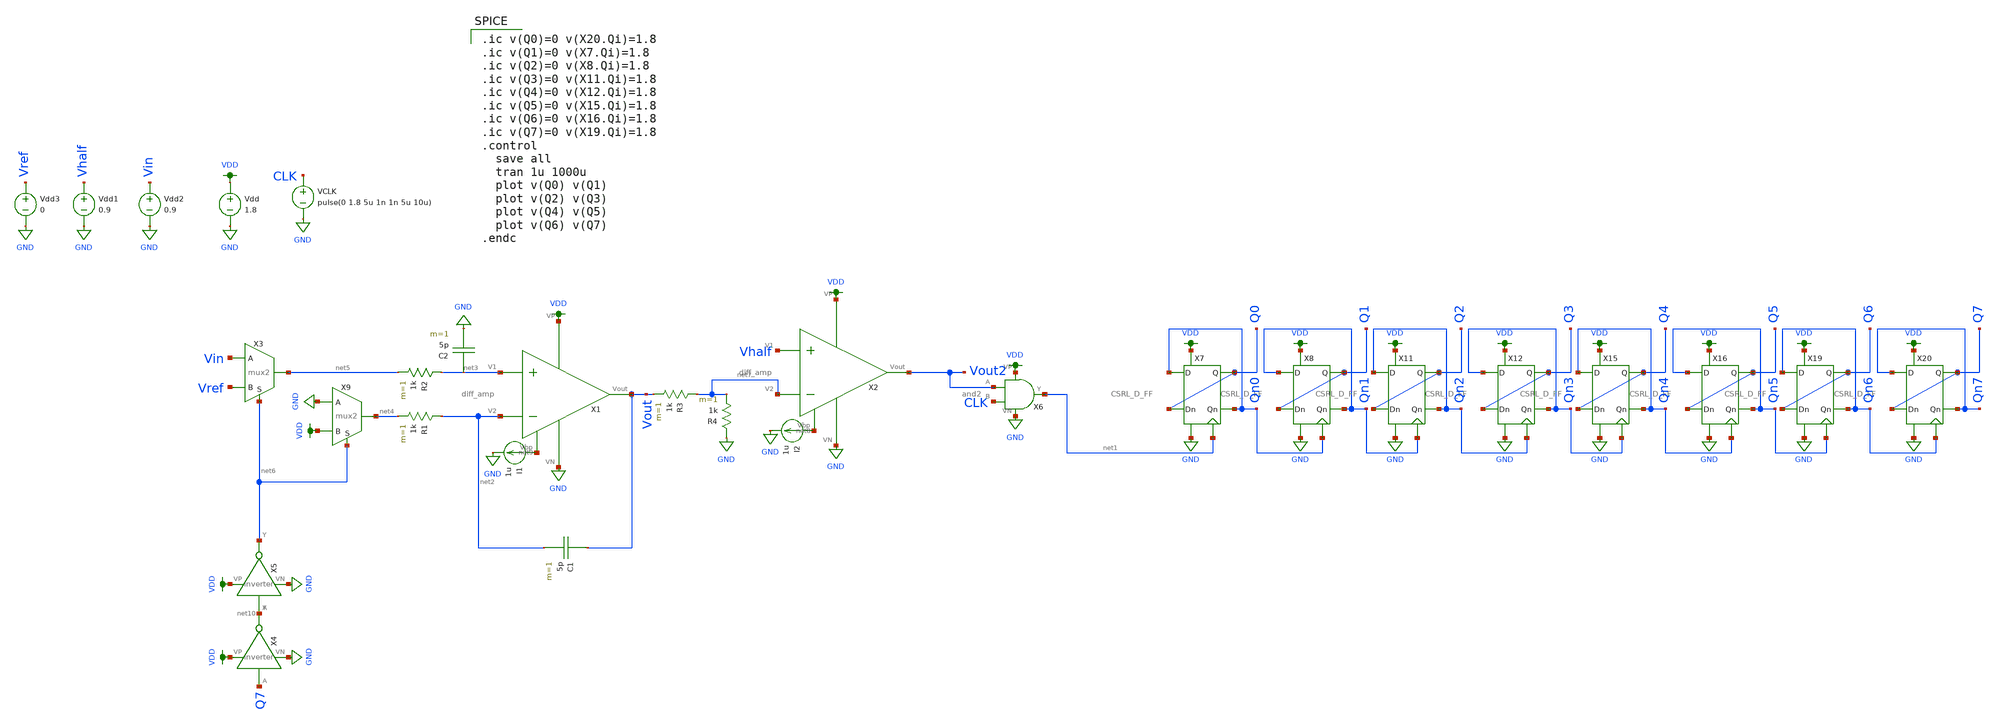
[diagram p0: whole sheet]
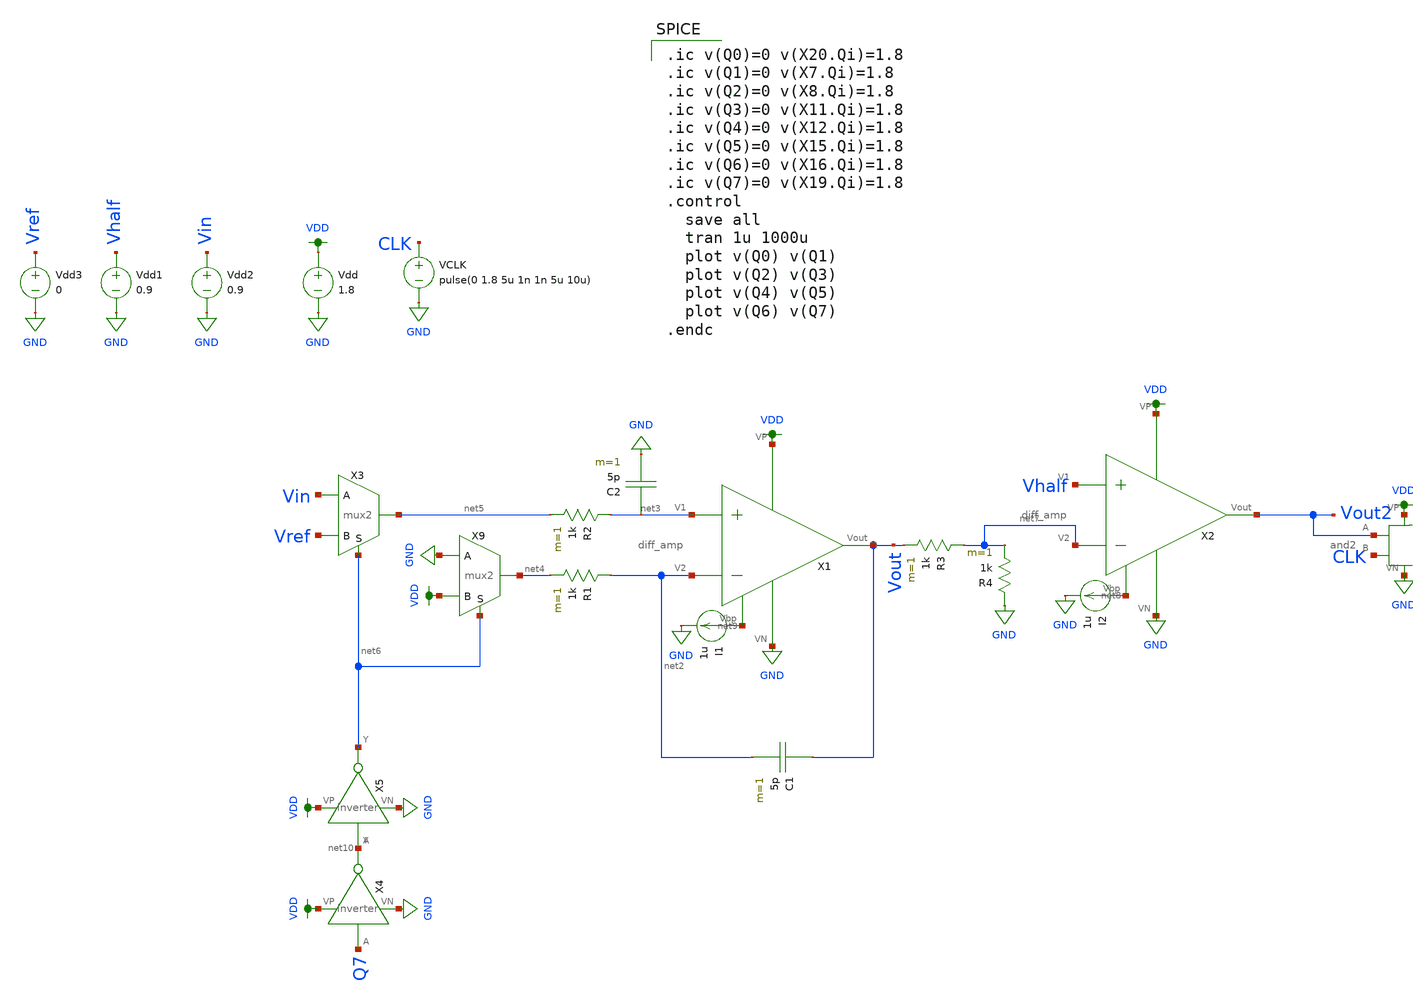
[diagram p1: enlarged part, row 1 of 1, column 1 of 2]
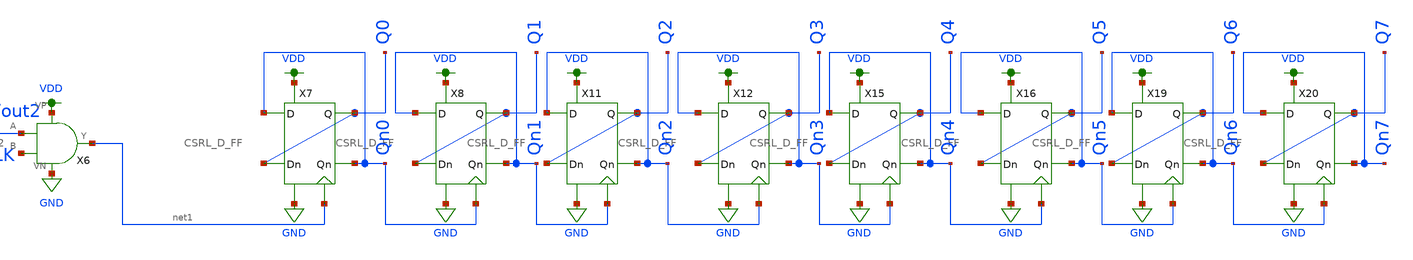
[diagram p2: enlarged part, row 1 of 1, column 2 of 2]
** sch_path: schematic/archive/double-slope-thomas.sch
**.subckt double-slope-thomas
X2 VDD net8 Vout2 Vhalf net7 GND diff_amp
Vdd VDD GND 1.8
VCLK CLK GND pulse(0 1.8 5u 1n 1n 5u 10u)
Vdd1 Vhalf GND 0.9
Vdd2 Vin GND 0.9
X7 Q0 Qn0 Qn0 Q0 GND VDD net1 CSRL_D_FF
X8 Q1 Qn1 Qn1 Q1 GND VDD Qn0 CSRL_D_FF
X11 Q2 Qn2 Qn2 Q2 GND VDD Qn1 CSRL_D_FF
X12 Q3 Qn3 Qn3 Q3 GND VDD Qn2 CSRL_D_FF
X15 Q4 Qn4 Qn4 Q4 GND VDD Qn3 CSRL_D_FF
X16 Q5 Qn5 Qn5 Q5 GND VDD Qn4 CSRL_D_FF
X19 Q6 Qn6 Qn6 Q6 GND VDD Qn5 CSRL_D_FF
X20 Q7 Qn7 Qn7 Q7 GND VDD Qn6 CSRL_D_FF
I2 net8 GND 1u
C1 Vout net2 5p m=1
X1 VDD net9 Vout net3 net2 GND diff_amp
R1 net2 net4 1k m=1
C2 net3 GND 5p m=1
R2 net3 net5 1k m=1
I1 net9 GND 1u
X3 net5 Vin Vref net6 mux2
Vdd3 Vref GND 0
X4 Q7 net10 VDD GND inverter
X5 net10 net6 VDD GND inverter
X6 VDD Vout2 GND net1 CLK and2
X9 net4 GND VDD net6 mux2
R3 net7 Vout 1k m=1
R4 GND net7 1k m=1
**** begin user architecture code

.ic v(Q0)=0 v(X20.Qi)=1.8
.ic v(Q1)=0 v(X7.Qi)=1.8
.ic v(Q2)=0 v(X8.Qi)=1.8
.ic v(Q3)=0 v(X11.Qi)=1.8
.ic v(Q4)=0 v(X12.Qi)=1.8
.ic v(Q5)=0 v(X15.Qi)=1.8
.ic v(Q6)=0 v(X16.Qi)=1.8
.ic v(Q7)=0 v(X19.Qi)=1.8
.control
  save all
  tran 1u 1000u
  plot v(Q0) v(Q1)
  plot v(Q2) v(Q3)
  plot v(Q4) v(Q5)
  plot v(Q6) v(Q7)
.endc


.option wnflag=1
.param MC_SWITCH=0.0
.lib ~/skywater/skywater-pdk/libraries/sky130_fd_pr_ngspice/latest/models/sky130.lib.spice tt

**** end user architecture code
**.ends
.GLOBAL GND
.GLOBAL VDD
.end
